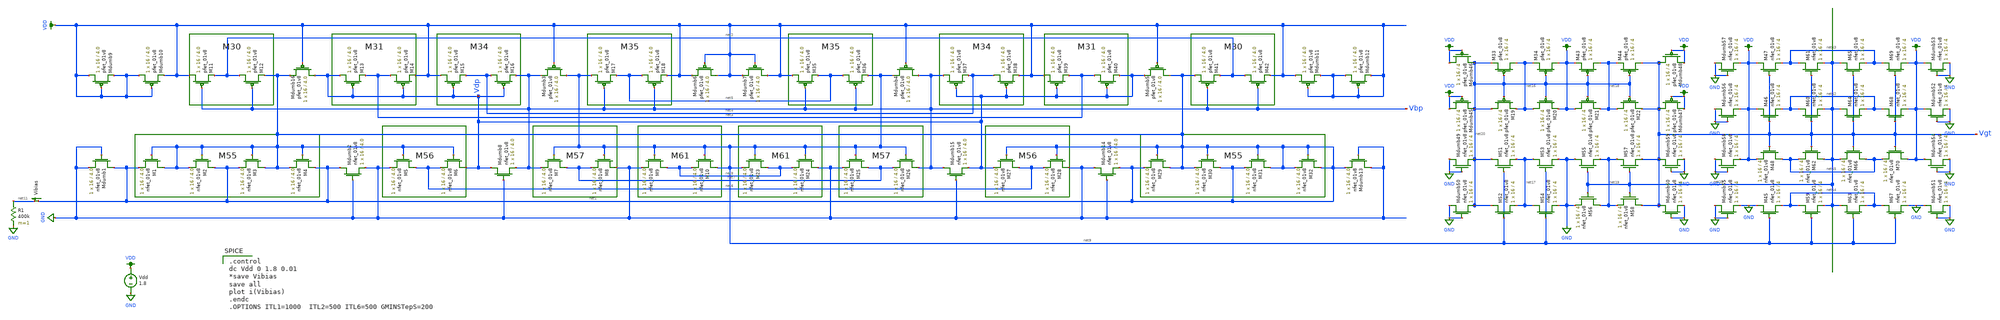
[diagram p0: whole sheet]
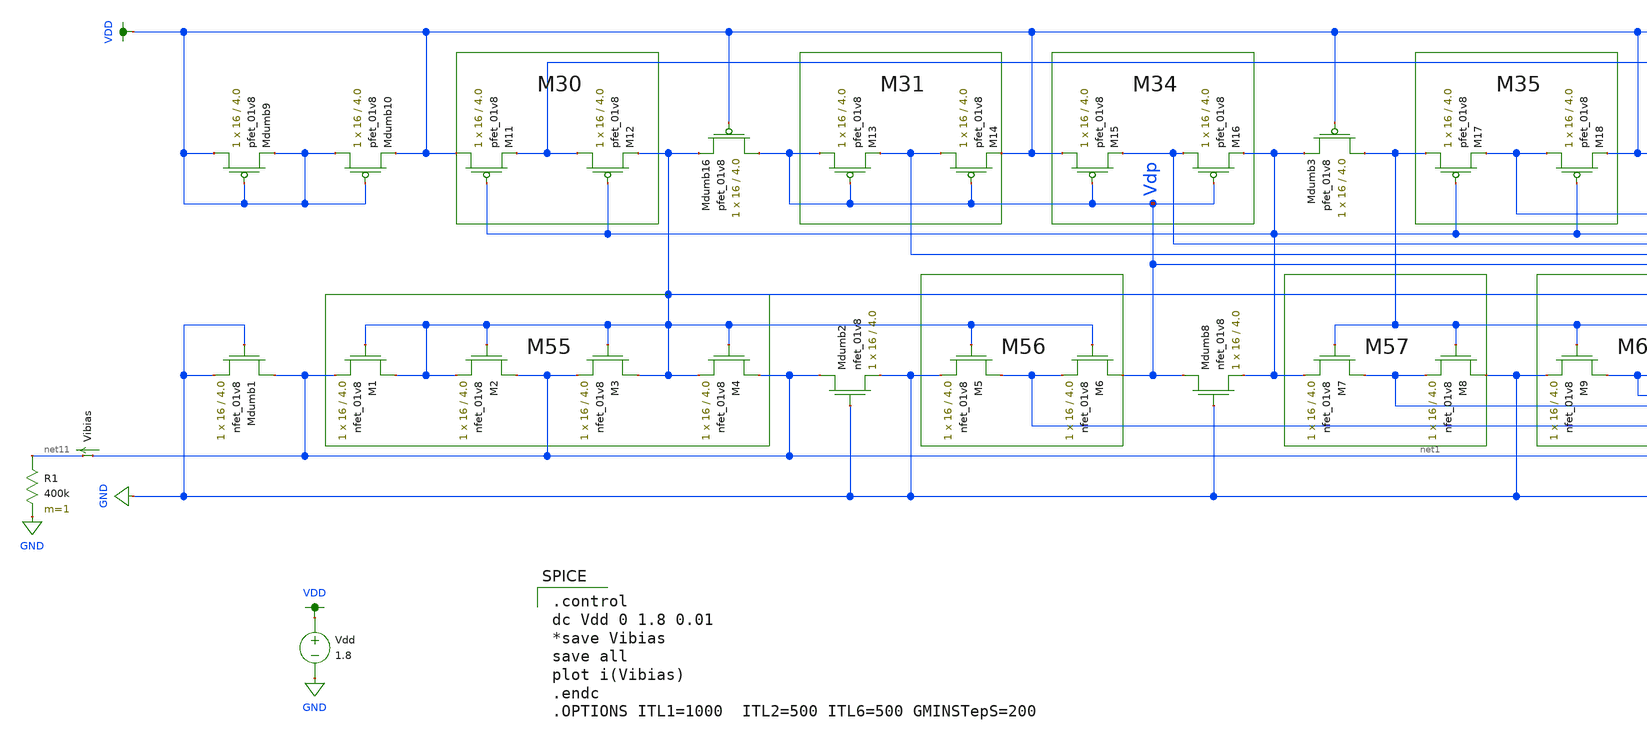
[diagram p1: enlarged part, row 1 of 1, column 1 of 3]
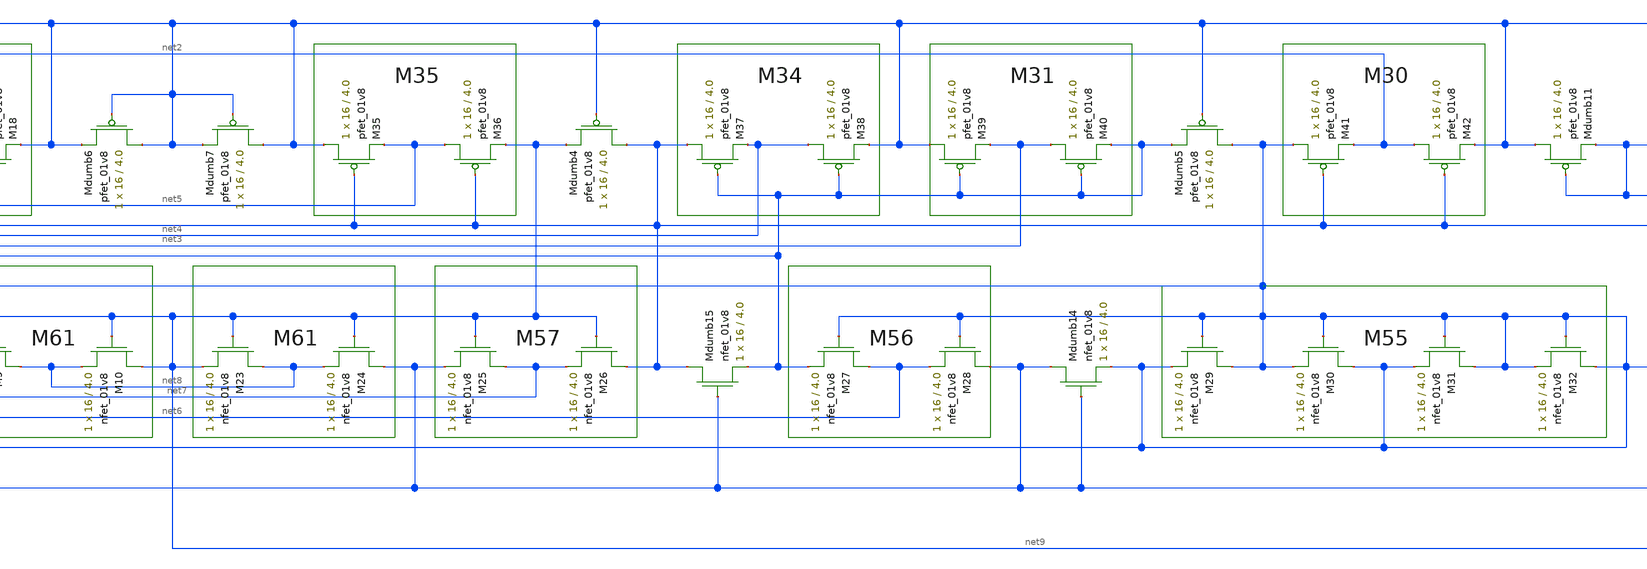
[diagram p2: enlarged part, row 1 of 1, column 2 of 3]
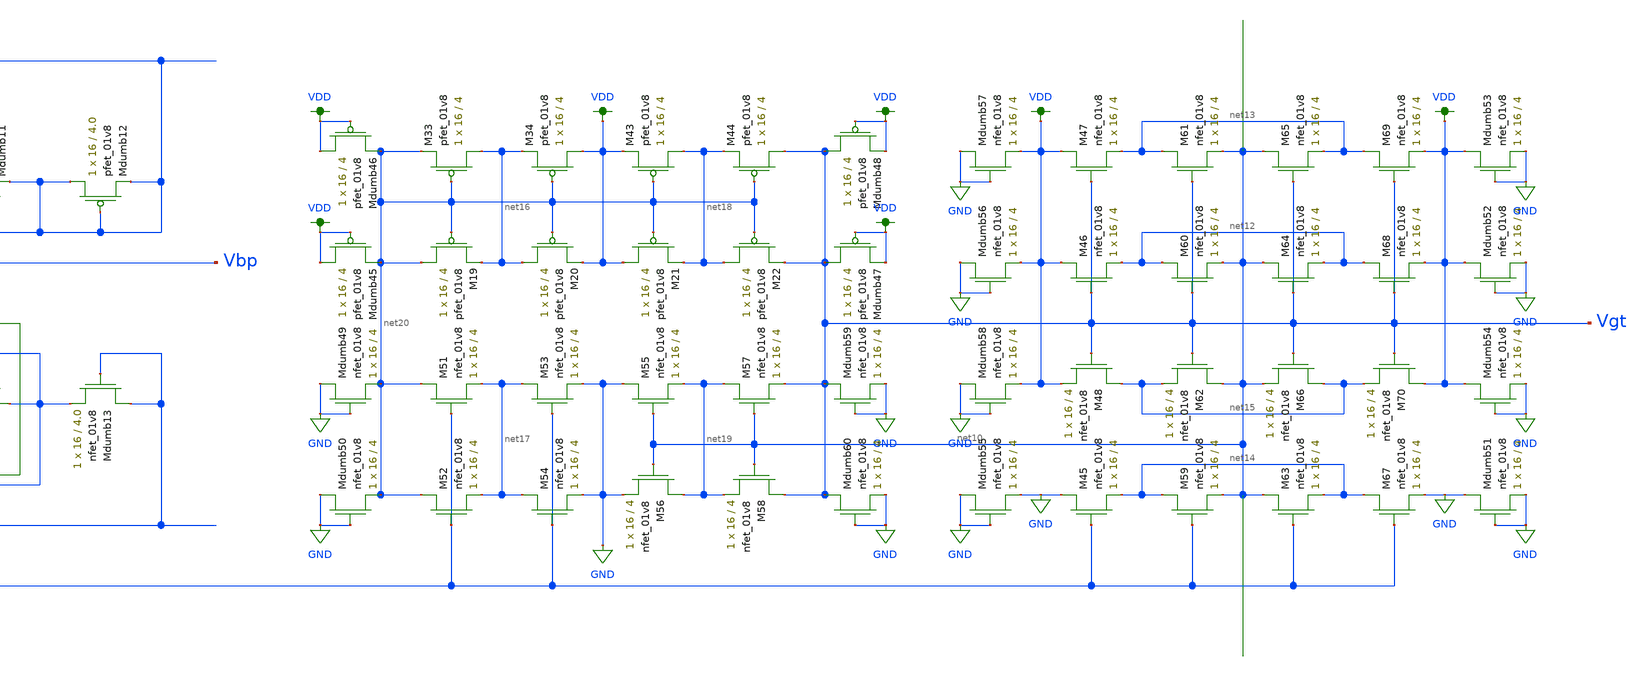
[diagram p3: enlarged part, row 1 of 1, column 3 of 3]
** sch_path: schematic/LDS/test/ibias_vgt.sch
**.subckt ibias_vgt
XM1 net1 net1 net1 GND sky130_fd_pr__nfet_01v8 L=4.0 W=16 nf=1 ad='int((nf+1)/2) * W/nf * 0.29' as='int((nf+2)/2) * W/nf * 0.29'
+ pd='2*int((nf+1)/2) * (W/nf + 0.29)' ps='2*int((nf+2)/2) * (W/nf + 0.29)' nrd='0.29 / W' nrs='0.29 / W'
+ sa=0 sb=0 sd=0 mult=1 m=1
XM2 net1 net1 net1 GND sky130_fd_pr__nfet_01v8 L=4.0 W=16 nf=1 ad='int((nf+1)/2) * W/nf * 0.29' as='int((nf+2)/2) * W/nf * 0.29'
+ pd='2*int((nf+1)/2) * (W/nf + 0.29)' ps='2*int((nf+2)/2) * (W/nf + 0.29)' nrd='0.29 / W' nrs='0.29 / W'
+ sa=0 sb=0 sd=0 mult=1 m=1
XM3 net1 net1 net1 GND sky130_fd_pr__nfet_01v8 L=4.0 W=16 nf=1 ad='int((nf+1)/2) * W/nf * 0.29' as='int((nf+2)/2) * W/nf * 0.29'
+ pd='2*int((nf+1)/2) * (W/nf + 0.29)' ps='2*int((nf+2)/2) * (W/nf + 0.29)' nrd='0.29 / W' nrs='0.29 / W'
+ sa=0 sb=0 sd=0 mult=1 m=1
XM4 net1 net1 net1 GND sky130_fd_pr__nfet_01v8 L=4.0 W=16 nf=1 ad='int((nf+1)/2) * W/nf * 0.29' as='int((nf+2)/2) * W/nf * 0.29'
+ pd='2*int((nf+1)/2) * (W/nf + 0.29)' ps='2*int((nf+2)/2) * (W/nf + 0.29)' nrd='0.29 / W' nrs='0.29 / W'
+ sa=0 sb=0 sd=0 mult=1 m=1
XM5 net6 net1 GND GND sky130_fd_pr__nfet_01v8 L=4.0 W=16 nf=1 ad='int((nf+1)/2) * W/nf * 0.29' as='int((nf+2)/2) * W/nf * 0.29'
+ pd='2*int((nf+1)/2) * (W/nf + 0.29)' ps='2*int((nf+2)/2) * (W/nf + 0.29)' nrd='0.29 / W' nrs='0.29 / W'
+ sa=0 sb=0 sd=0 mult=1 m=1
XM6 Vdp net1 net6 GND sky130_fd_pr__nfet_01v8 L=4.0 W=16 nf=1 ad='int((nf+1)/2) * W/nf * 0.29' as='int((nf+2)/2) * W/nf * 0.29'
+ pd='2*int((nf+1)/2) * (W/nf + 0.29)' ps='2*int((nf+2)/2) * (W/nf + 0.29)' nrd='0.29 / W' nrs='0.29 / W'
+ sa=0 sb=0 sd=0 mult=1 m=1
XM7 net7 net9 Vbp GND sky130_fd_pr__nfet_01v8 L=4.0 W=16 nf=1 ad='int((nf+1)/2) * W/nf * 0.29' as='int((nf+2)/2) * W/nf * 0.29'
+ pd='2*int((nf+1)/2) * (W/nf + 0.29)' ps='2*int((nf+2)/2) * (W/nf + 0.29)' nrd='0.29 / W' nrs='0.29 / W'
+ sa=0 sb=0 sd=0 mult=1 m=1
XM8 GND net9 net7 GND sky130_fd_pr__nfet_01v8 L=4.0 W=16 nf=1 ad='int((nf+1)/2) * W/nf * 0.29' as='int((nf+2)/2) * W/nf * 0.29'
+ pd='2*int((nf+1)/2) * (W/nf + 0.29)' ps='2*int((nf+2)/2) * (W/nf + 0.29)' nrd='0.29 / W' nrs='0.29 / W'
+ sa=0 sb=0 sd=0 mult=1 m=1
XM9 net8 net9 GND GND sky130_fd_pr__nfet_01v8 L=4.0 W=16 nf=1 ad='int((nf+1)/2) * W/nf * 0.29' as='int((nf+2)/2) * W/nf * 0.29'
+ pd='2*int((nf+1)/2) * (W/nf + 0.29)' ps='2*int((nf+2)/2) * (W/nf + 0.29)' nrd='0.29 / W' nrs='0.29 / W'
+ sa=0 sb=0 sd=0 mult=1 m=1
XM10 net9 net9 net8 GND sky130_fd_pr__nfet_01v8 L=4.0 W=16 nf=1 ad='int((nf+1)/2) * W/nf * 0.29' as='int((nf+2)/2) * W/nf * 0.29'
+ pd='2*int((nf+1)/2) * (W/nf + 0.29)' ps='2*int((nf+2)/2) * (W/nf + 0.29)' nrd='0.29 / W' nrs='0.29 / W'
+ sa=0 sb=0 sd=0 mult=1 m=1
XM11 VDD Vbp net2 VDD sky130_fd_pr__pfet_01v8 L=4.0 W=16 nf=1 ad='int((nf+1)/2) * W/nf * 0.29' as='int((nf+2)/2) * W/nf * 0.29'
+ pd='2*int((nf+1)/2) * (W/nf + 0.29)' ps='2*int((nf+2)/2) * (W/nf + 0.29)' nrd='0.29 / W' nrs='0.29 / W'
+ sa=0 sb=0 sd=0 mult=1 m=1
XM12 net2 Vbp net1 VDD sky130_fd_pr__pfet_01v8 L=4.0 W=16 nf=1 ad='int((nf+1)/2) * W/nf * 0.29' as='int((nf+2)/2) * W/nf * 0.29'
+ pd='2*int((nf+1)/2) * (W/nf + 0.29)' ps='2*int((nf+2)/2) * (W/nf + 0.29)' nrd='0.29 / W' nrs='0.29 / W'
+ sa=0 sb=0 sd=0 mult=1 m=1
XM13 Vdp Vdp net3 VDD sky130_fd_pr__pfet_01v8 L=4.0 W=16 nf=1 ad='int((nf+1)/2) * W/nf * 0.29' as='int((nf+2)/2) * W/nf * 0.29'
+ pd='2*int((nf+1)/2) * (W/nf + 0.29)' ps='2*int((nf+2)/2) * (W/nf + 0.29)' nrd='0.29 / W' nrs='0.29 / W'
+ sa=0 sb=0 sd=0 mult=1 m=1
XM14 net3 Vdp VDD VDD sky130_fd_pr__pfet_01v8 L=4.0 W=16 nf=1 ad='int((nf+1)/2) * W/nf * 0.29' as='int((nf+2)/2) * W/nf * 0.29'
+ pd='2*int((nf+1)/2) * (W/nf + 0.29)' ps='2*int((nf+2)/2) * (W/nf + 0.29)' nrd='0.29 / W' nrs='0.29 / W'
+ sa=0 sb=0 sd=0 mult=1 m=1
XM15 VDD Vdp net4 VDD sky130_fd_pr__pfet_01v8 L=4.0 W=16 nf=1 ad='int((nf+1)/2) * W/nf * 0.29' as='int((nf+2)/2) * W/nf * 0.29'
+ pd='2*int((nf+1)/2) * (W/nf + 0.29)' ps='2*int((nf+2)/2) * (W/nf + 0.29)' nrd='0.29 / W' nrs='0.29 / W'
+ sa=0 sb=0 sd=0 mult=1 m=1
XM16 net4 Vdp Vbp VDD sky130_fd_pr__pfet_01v8 L=4.0 W=16 nf=1 ad='int((nf+1)/2) * W/nf * 0.29' as='int((nf+2)/2) * W/nf * 0.29'
+ pd='2*int((nf+1)/2) * (W/nf + 0.29)' ps='2*int((nf+2)/2) * (W/nf + 0.29)' nrd='0.29 / W' nrs='0.29 / W'
+ sa=0 sb=0 sd=0 mult=1 m=1
XM17 net9 Vbp net5 VDD sky130_fd_pr__pfet_01v8 L=4.0 W=16 nf=1 ad='int((nf+1)/2) * W/nf * 0.29' as='int((nf+2)/2) * W/nf * 0.29'
+ pd='2*int((nf+1)/2) * (W/nf + 0.29)' ps='2*int((nf+2)/2) * (W/nf + 0.29)' nrd='0.29 / W' nrs='0.29 / W'
+ sa=0 sb=0 sd=0 mult=1 m=1
XM18 net5 Vbp VDD VDD sky130_fd_pr__pfet_01v8 L=4.0 W=16 nf=1 ad='int((nf+1)/2) * W/nf * 0.29' as='int((nf+2)/2) * W/nf * 0.29'
+ pd='2*int((nf+1)/2) * (W/nf + 0.29)' ps='2*int((nf+2)/2) * (W/nf + 0.29)' nrd='0.29 / W' nrs='0.29 / W'
+ sa=0 sb=0 sd=0 mult=1 m=1
XMdumb16 Vdp VDD net1 VDD sky130_fd_pr__pfet_01v8 L=4.0 W=16 nf=1 ad='int((nf+1)/2) * W/nf * 0.29' as='int((nf+2)/2) * W/nf * 0.29'
+ pd='2*int((nf+1)/2) * (W/nf + 0.29)' ps='2*int((nf+2)/2) * (W/nf + 0.29)' nrd='0.29 / W' nrs='0.29 / W'
+ sa=0 sb=0 sd=0 mult=1 m=1
XMdumb3 net9 VDD Vbp VDD sky130_fd_pr__pfet_01v8 L=4.0 W=16 nf=1 ad='int((nf+1)/2) * W/nf * 0.29' as='int((nf+2)/2) * W/nf * 0.29'
+ pd='2*int((nf+1)/2) * (W/nf + 0.29)' ps='2*int((nf+2)/2) * (W/nf + 0.29)' nrd='0.29 / W' nrs='0.29 / W'
+ sa=0 sb=0 sd=0 mult=1 m=1
XMdumb2 net1 GND GND GND sky130_fd_pr__nfet_01v8 L=4.0 W=16 nf=1 ad='int((nf+1)/2) * W/nf * 0.29' as='int((nf+2)/2) * W/nf * 0.29'
+ pd='2*int((nf+1)/2) * (W/nf + 0.29)' ps='2*int((nf+2)/2) * (W/nf + 0.29)' nrd='0.29 / W' nrs='0.29 / W'
+ sa=0 sb=0 sd=0 mult=1 m=1
XMdumb8 Vdp GND Vbp GND sky130_fd_pr__nfet_01v8 L=4.0 W=16 nf=1 ad='int((nf+1)/2) * W/nf * 0.29' as='int((nf+2)/2) * W/nf * 0.29'
+ pd='2*int((nf+1)/2) * (W/nf + 0.29)' ps='2*int((nf+2)/2) * (W/nf + 0.29)' nrd='0.29 / W' nrs='0.29 / W'
+ sa=0 sb=0 sd=0 mult=1 m=1
XM23 net8 net9 net9 GND sky130_fd_pr__nfet_01v8 L=4.0 W=16 nf=1 ad='int((nf+1)/2) * W/nf * 0.29' as='int((nf+2)/2) * W/nf * 0.29'
+ pd='2*int((nf+1)/2) * (W/nf + 0.29)' ps='2*int((nf+2)/2) * (W/nf + 0.29)' nrd='0.29 / W' nrs='0.29 / W'
+ sa=0 sb=0 sd=0 mult=1 m=1
XM24 GND net9 net8 GND sky130_fd_pr__nfet_01v8 L=4.0 W=16 nf=1 ad='int((nf+1)/2) * W/nf * 0.29' as='int((nf+2)/2) * W/nf * 0.29'
+ pd='2*int((nf+1)/2) * (W/nf + 0.29)' ps='2*int((nf+2)/2) * (W/nf + 0.29)' nrd='0.29 / W' nrs='0.29 / W'
+ sa=0 sb=0 sd=0 mult=1 m=1
XM25 net7 net9 GND GND sky130_fd_pr__nfet_01v8 L=4.0 W=16 nf=1 ad='int((nf+1)/2) * W/nf * 0.29' as='int((nf+2)/2) * W/nf * 0.29'
+ pd='2*int((nf+1)/2) * (W/nf + 0.29)' ps='2*int((nf+2)/2) * (W/nf + 0.29)' nrd='0.29 / W' nrs='0.29 / W'
+ sa=0 sb=0 sd=0 mult=1 m=1
XM26 Vbp net9 net7 GND sky130_fd_pr__nfet_01v8 L=4.0 W=16 nf=1 ad='int((nf+1)/2) * W/nf * 0.29' as='int((nf+2)/2) * W/nf * 0.29'
+ pd='2*int((nf+1)/2) * (W/nf + 0.29)' ps='2*int((nf+2)/2) * (W/nf + 0.29)' nrd='0.29 / W' nrs='0.29 / W'
+ sa=0 sb=0 sd=0 mult=1 m=1
XM27 net6 net1 Vdp GND sky130_fd_pr__nfet_01v8 L=4.0 W=16 nf=1 ad='int((nf+1)/2) * W/nf * 0.29' as='int((nf+2)/2) * W/nf * 0.29'
+ pd='2*int((nf+1)/2) * (W/nf + 0.29)' ps='2*int((nf+2)/2) * (W/nf + 0.29)' nrd='0.29 / W' nrs='0.29 / W'
+ sa=0 sb=0 sd=0 mult=1 m=1
XM28 GND net1 net6 GND sky130_fd_pr__nfet_01v8 L=4.0 W=16 nf=1 ad='int((nf+1)/2) * W/nf * 0.29' as='int((nf+2)/2) * W/nf * 0.29'
+ pd='2*int((nf+1)/2) * (W/nf + 0.29)' ps='2*int((nf+2)/2) * (W/nf + 0.29)' nrd='0.29 / W' nrs='0.29 / W'
+ sa=0 sb=0 sd=0 mult=1 m=1
XM29 net1 net1 net1 GND sky130_fd_pr__nfet_01v8 L=4.0 W=16 nf=1 ad='int((nf+1)/2) * W/nf * 0.29' as='int((nf+2)/2) * W/nf * 0.29'
+ pd='2*int((nf+1)/2) * (W/nf + 0.29)' ps='2*int((nf+2)/2) * (W/nf + 0.29)' nrd='0.29 / W' nrs='0.29 / W'
+ sa=0 sb=0 sd=0 mult=1 m=1
XM30 net1 net1 net1 GND sky130_fd_pr__nfet_01v8 L=4.0 W=16 nf=1 ad='int((nf+1)/2) * W/nf * 0.29' as='int((nf+2)/2) * W/nf * 0.29'
+ pd='2*int((nf+1)/2) * (W/nf + 0.29)' ps='2*int((nf+2)/2) * (W/nf + 0.29)' nrd='0.29 / W' nrs='0.29 / W'
+ sa=0 sb=0 sd=0 mult=1 m=1
XM31 net1 net1 net1 GND sky130_fd_pr__nfet_01v8 L=4.0 W=16 nf=1 ad='int((nf+1)/2) * W/nf * 0.29' as='int((nf+2)/2) * W/nf * 0.29'
+ pd='2*int((nf+1)/2) * (W/nf + 0.29)' ps='2*int((nf+2)/2) * (W/nf + 0.29)' nrd='0.29 / W' nrs='0.29 / W'
+ sa=0 sb=0 sd=0 mult=1 m=1
XM32 net1 net1 net1 GND sky130_fd_pr__nfet_01v8 L=4.0 W=16 nf=1 ad='int((nf+1)/2) * W/nf * 0.29' as='int((nf+2)/2) * W/nf * 0.29'
+ pd='2*int((nf+1)/2) * (W/nf + 0.29)' ps='2*int((nf+2)/2) * (W/nf + 0.29)' nrd='0.29 / W' nrs='0.29 / W'
+ sa=0 sb=0 sd=0 mult=1 m=1
XMdumb15 Vbp GND Vdp GND sky130_fd_pr__nfet_01v8 L=4.0 W=16 nf=1 ad='int((nf+1)/2) * W/nf * 0.29' as='int((nf+2)/2) * W/nf * 0.29'
+ pd='2*int((nf+1)/2) * (W/nf + 0.29)' ps='2*int((nf+2)/2) * (W/nf + 0.29)' nrd='0.29 / W' nrs='0.29 / W'
+ sa=0 sb=0 sd=0 mult=1 m=1
XMdumb14 GND GND net1 GND sky130_fd_pr__nfet_01v8 L=4.0 W=16 nf=1 ad='int((nf+1)/2) * W/nf * 0.29' as='int((nf+2)/2) * W/nf * 0.29'
+ pd='2*int((nf+1)/2) * (W/nf + 0.29)' ps='2*int((nf+2)/2) * (W/nf + 0.29)' nrd='0.29 / W' nrs='0.29 / W'
+ sa=0 sb=0 sd=0 mult=1 m=1
XM35 VDD Vbp net5 VDD sky130_fd_pr__pfet_01v8 L=4.0 W=16 nf=1 ad='int((nf+1)/2) * W/nf * 0.29' as='int((nf+2)/2) * W/nf * 0.29'
+ pd='2*int((nf+1)/2) * (W/nf + 0.29)' ps='2*int((nf+2)/2) * (W/nf + 0.29)' nrd='0.29 / W' nrs='0.29 / W'
+ sa=0 sb=0 sd=0 mult=1 m=1
XM36 net5 Vbp net9 VDD sky130_fd_pr__pfet_01v8 L=4.0 W=16 nf=1 ad='int((nf+1)/2) * W/nf * 0.29' as='int((nf+2)/2) * W/nf * 0.29'
+ pd='2*int((nf+1)/2) * (W/nf + 0.29)' ps='2*int((nf+2)/2) * (W/nf + 0.29)' nrd='0.29 / W' nrs='0.29 / W'
+ sa=0 sb=0 sd=0 mult=1 m=1
XM37 Vbp Vdp net4 VDD sky130_fd_pr__pfet_01v8 L=4.0 W=16 nf=1 ad='int((nf+1)/2) * W/nf * 0.29' as='int((nf+2)/2) * W/nf * 0.29'
+ pd='2*int((nf+1)/2) * (W/nf + 0.29)' ps='2*int((nf+2)/2) * (W/nf + 0.29)' nrd='0.29 / W' nrs='0.29 / W'
+ sa=0 sb=0 sd=0 mult=1 m=1
XM38 net4 Vdp VDD VDD sky130_fd_pr__pfet_01v8 L=4.0 W=16 nf=1 ad='int((nf+1)/2) * W/nf * 0.29' as='int((nf+2)/2) * W/nf * 0.29'
+ pd='2*int((nf+1)/2) * (W/nf + 0.29)' ps='2*int((nf+2)/2) * (W/nf + 0.29)' nrd='0.29 / W' nrs='0.29 / W'
+ sa=0 sb=0 sd=0 mult=1 m=1
XM39 VDD Vdp net3 VDD sky130_fd_pr__pfet_01v8 L=4.0 W=16 nf=1 ad='int((nf+1)/2) * W/nf * 0.29' as='int((nf+2)/2) * W/nf * 0.29'
+ pd='2*int((nf+1)/2) * (W/nf + 0.29)' ps='2*int((nf+2)/2) * (W/nf + 0.29)' nrd='0.29 / W' nrs='0.29 / W'
+ sa=0 sb=0 sd=0 mult=1 m=1
XM40 net3 Vdp Vdp VDD sky130_fd_pr__pfet_01v8 L=4.0 W=16 nf=1 ad='int((nf+1)/2) * W/nf * 0.29' as='int((nf+2)/2) * W/nf * 0.29'
+ pd='2*int((nf+1)/2) * (W/nf + 0.29)' ps='2*int((nf+2)/2) * (W/nf + 0.29)' nrd='0.29 / W' nrs='0.29 / W'
+ sa=0 sb=0 sd=0 mult=1 m=1
XM41 net1 Vbp net2 VDD sky130_fd_pr__pfet_01v8 L=4.0 W=16 nf=1 ad='int((nf+1)/2) * W/nf * 0.29' as='int((nf+2)/2) * W/nf * 0.29'
+ pd='2*int((nf+1)/2) * (W/nf + 0.29)' ps='2*int((nf+2)/2) * (W/nf + 0.29)' nrd='0.29 / W' nrs='0.29 / W'
+ sa=0 sb=0 sd=0 mult=1 m=1
XM42 net2 Vbp VDD VDD sky130_fd_pr__pfet_01v8 L=4.0 W=16 nf=1 ad='int((nf+1)/2) * W/nf * 0.29' as='int((nf+2)/2) * W/nf * 0.29'
+ pd='2*int((nf+1)/2) * (W/nf + 0.29)' ps='2*int((nf+2)/2) * (W/nf + 0.29)' nrd='0.29 / W' nrs='0.29 / W'
+ sa=0 sb=0 sd=0 mult=1 m=1
XMdumb4 Vbp VDD net9 VDD sky130_fd_pr__pfet_01v8 L=4.0 W=16 nf=1 ad='int((nf+1)/2) * W/nf * 0.29' as='int((nf+2)/2) * W/nf * 0.29'
+ pd='2*int((nf+1)/2) * (W/nf + 0.29)' ps='2*int((nf+2)/2) * (W/nf + 0.29)' nrd='0.29 / W' nrs='0.29 / W'
+ sa=0 sb=0 sd=0 mult=1 m=1
XMdumb5 net1 VDD Vdp VDD sky130_fd_pr__pfet_01v8 L=4.0 W=16 nf=1 ad='int((nf+1)/2) * W/nf * 0.29' as='int((nf+2)/2) * W/nf * 0.29'
+ pd='2*int((nf+1)/2) * (W/nf + 0.29)' ps='2*int((nf+2)/2) * (W/nf + 0.29)' nrd='0.29 / W' nrs='0.29 / W'
+ sa=0 sb=0 sd=0 mult=1 m=1
XMdumb6 VDD VDD VDD VDD sky130_fd_pr__pfet_01v8 L=4.0 W=16 nf=1 ad='int((nf+1)/2) * W/nf * 0.29' as='int((nf+2)/2) * W/nf * 0.29'
+ pd='2*int((nf+1)/2) * (W/nf + 0.29)' ps='2*int((nf+2)/2) * (W/nf + 0.29)' nrd='0.29 / W' nrs='0.29 / W'
+ sa=0 sb=0 sd=0 mult=1 m=1
XMdumb7 VDD VDD VDD VDD sky130_fd_pr__pfet_01v8 L=4.0 W=16 nf=1 ad='int((nf+1)/2) * W/nf * 0.29' as='int((nf+2)/2) * W/nf * 0.29'
+ pd='2*int((nf+1)/2) * (W/nf + 0.29)' ps='2*int((nf+2)/2) * (W/nf + 0.29)' nrd='0.29 / W' nrs='0.29 / W'
+ sa=0 sb=0 sd=0 mult=1 m=1
XMdumb11 VDD VDD VDD VDD sky130_fd_pr__pfet_01v8 L=4.0 W=16 nf=1 ad='int((nf+1)/2) * W/nf * 0.29' as='int((nf+2)/2) * W/nf * 0.29'
+ pd='2*int((nf+1)/2) * (W/nf + 0.29)' ps='2*int((nf+2)/2) * (W/nf + 0.29)' nrd='0.29 / W' nrs='0.29 / W'
+ sa=0 sb=0 sd=0 mult=1 m=1
XMdumb12 VDD VDD VDD VDD sky130_fd_pr__pfet_01v8 L=4.0 W=16 nf=1 ad='int((nf+1)/2) * W/nf * 0.29' as='int((nf+2)/2) * W/nf * 0.29'
+ pd='2*int((nf+1)/2) * (W/nf + 0.29)' ps='2*int((nf+2)/2) * (W/nf + 0.29)' nrd='0.29 / W' nrs='0.29 / W'
+ sa=0 sb=0 sd=0 mult=1 m=1
XMdumb13 GND GND net1 GND sky130_fd_pr__nfet_01v8 L=4.0 W=16 nf=1 ad='int((nf+1)/2) * W/nf * 0.29' as='int((nf+2)/2) * W/nf * 0.29'
+ pd='2*int((nf+1)/2) * (W/nf + 0.29)' ps='2*int((nf+2)/2) * (W/nf + 0.29)' nrd='0.29 / W' nrs='0.29 / W'
+ sa=0 sb=0 sd=0 mult=1 m=1
XMdumb1 net1 GND GND GND sky130_fd_pr__nfet_01v8 L=4.0 W=16 nf=1 ad='int((nf+1)/2) * W/nf * 0.29' as='int((nf+2)/2) * W/nf * 0.29'
+ pd='2*int((nf+1)/2) * (W/nf + 0.29)' ps='2*int((nf+2)/2) * (W/nf + 0.29)' nrd='0.29 / W' nrs='0.29 / W'
+ sa=0 sb=0 sd=0 mult=1 m=1
XMdumb10 VDD VDD VDD VDD sky130_fd_pr__pfet_01v8 L=4.0 W=16 nf=1 ad='int((nf+1)/2) * W/nf * 0.29' as='int((nf+2)/2) * W/nf * 0.29'
+ pd='2*int((nf+1)/2) * (W/nf + 0.29)' ps='2*int((nf+2)/2) * (W/nf + 0.29)' nrd='0.29 / W' nrs='0.29 / W'
+ sa=0 sb=0 sd=0 mult=1 m=1
XMdumb9 VDD VDD VDD VDD sky130_fd_pr__pfet_01v8 L=4.0 W=16 nf=1 ad='int((nf+1)/2) * W/nf * 0.29' as='int((nf+2)/2) * W/nf * 0.29'
+ pd='2*int((nf+1)/2) * (W/nf + 0.29)' ps='2*int((nf+2)/2) * (W/nf + 0.29)' nrd='0.29 / W' nrs='0.29 / W'
+ sa=0 sb=0 sd=0 mult=1 m=1
Vdd VDD GND 1.8
R1 net11 GND 400k m=1
Vibias net1 net11 0
.save i(vibias)
XM45 GND net9 net14 GND sky130_fd_pr__nfet_01v8 L=4 W=16 nf=1 ad='int((nf+1)/2) * W/nf * 0.29' as='int((nf+2)/2) * W/nf * 0.29'
+ pd='2*int((nf+1)/2) * (W/nf + 0.29)' ps='2*int((nf+2)/2) * (W/nf + 0.29)' nrd='0.29 / W' nrs='0.29 / W'
+ sa=0 sb=0 sd=0 mult=1 m=1
XM46 VDD Vgt net12 GND sky130_fd_pr__nfet_01v8 L=4 W=16 nf=1 ad='int((nf+1)/2) * W/nf * 0.29' as='int((nf+2)/2) * W/nf * 0.29'
+ pd='2*int((nf+1)/2) * (W/nf + 0.29)' ps='2*int((nf+2)/2) * (W/nf + 0.29)' nrd='0.29 / W' nrs='0.29 / W'
+ sa=0 sb=0 sd=0 mult=1 m=1
XM47 VDD Vgt net13 GND sky130_fd_pr__nfet_01v8 L=4 W=16 nf=1 ad='int((nf+1)/2) * W/nf * 0.29' as='int((nf+2)/2) * W/nf * 0.29'
+ pd='2*int((nf+1)/2) * (W/nf + 0.29)' ps='2*int((nf+2)/2) * (W/nf + 0.29)' nrd='0.29 / W' nrs='0.29 / W'
+ sa=0 sb=0 sd=0 mult=1 m=1
XM48 net15 Vgt VDD GND sky130_fd_pr__nfet_01v8 L=4 W=16 nf=1 ad='int((nf+1)/2) * W/nf * 0.29' as='int((nf+2)/2) * W/nf * 0.29'
+ pd='2*int((nf+1)/2) * (W/nf + 0.29)' ps='2*int((nf+2)/2) * (W/nf + 0.29)' nrd='0.29 / W' nrs='0.29 / W'
+ sa=0 sb=0 sd=0 mult=1 m=1
XMdumb51 GND GND GND GND sky130_fd_pr__nfet_01v8 L=4 W=16 nf=1 ad='int((nf+1)/2) * W/nf * 0.29' as='int((nf+2)/2) * W/nf * 0.29'
+ pd='2*int((nf+1)/2) * (W/nf + 0.29)' ps='2*int((nf+2)/2) * (W/nf + 0.29)' nrd='0.29 / W' nrs='0.29 / W'
+ sa=0 sb=0 sd=0 mult=1 m=1
XMdumb52 VDD GND GND GND sky130_fd_pr__nfet_01v8 L=4 W=16 nf=1 ad='int((nf+1)/2) * W/nf * 0.29' as='int((nf+2)/2) * W/nf * 0.29'
+ pd='2*int((nf+1)/2) * (W/nf + 0.29)' ps='2*int((nf+2)/2) * (W/nf + 0.29)' nrd='0.29 / W' nrs='0.29 / W'
+ sa=0 sb=0 sd=0 mult=1 m=1
XMdumb53 VDD GND GND GND sky130_fd_pr__nfet_01v8 L=4 W=16 nf=1 ad='int((nf+1)/2) * W/nf * 0.29' as='int((nf+2)/2) * W/nf * 0.29'
+ pd='2*int((nf+1)/2) * (W/nf + 0.29)' ps='2*int((nf+2)/2) * (W/nf + 0.29)' nrd='0.29 / W' nrs='0.29 / W'
+ sa=0 sb=0 sd=0 mult=1 m=1
XMdumb54 VDD GND GND GND sky130_fd_pr__nfet_01v8 L=4 W=16 nf=1 ad='int((nf+1)/2) * W/nf * 0.29' as='int((nf+2)/2) * W/nf * 0.29'
+ pd='2*int((nf+1)/2) * (W/nf + 0.29)' ps='2*int((nf+2)/2) * (W/nf + 0.29)' nrd='0.29 / W' nrs='0.29 / W'
+ sa=0 sb=0 sd=0 mult=1 m=1
XMdumb55 GND GND GND GND sky130_fd_pr__nfet_01v8 L=4 W=16 nf=1 ad='int((nf+1)/2) * W/nf * 0.29' as='int((nf+2)/2) * W/nf * 0.29'
+ pd='2*int((nf+1)/2) * (W/nf + 0.29)' ps='2*int((nf+2)/2) * (W/nf + 0.29)' nrd='0.29 / W' nrs='0.29 / W'
+ sa=0 sb=0 sd=0 mult=1 m=1
XMdumb56 GND GND VDD GND sky130_fd_pr__nfet_01v8 L=4 W=16 nf=1 ad='int((nf+1)/2) * W/nf * 0.29' as='int((nf+2)/2) * W/nf * 0.29'
+ pd='2*int((nf+1)/2) * (W/nf + 0.29)' ps='2*int((nf+2)/2) * (W/nf + 0.29)' nrd='0.29 / W' nrs='0.29 / W'
+ sa=0 sb=0 sd=0 mult=1 m=1
XMdumb57 GND GND VDD GND sky130_fd_pr__nfet_01v8 L=4 W=16 nf=1 ad='int((nf+1)/2) * W/nf * 0.29' as='int((nf+2)/2) * W/nf * 0.29'
+ pd='2*int((nf+1)/2) * (W/nf + 0.29)' ps='2*int((nf+2)/2) * (W/nf + 0.29)' nrd='0.29 / W' nrs='0.29 / W'
+ sa=0 sb=0 sd=0 mult=1 m=1
XMdumb58 GND GND VDD GND sky130_fd_pr__nfet_01v8 L=4 W=16 nf=1 ad='int((nf+1)/2) * W/nf * 0.29' as='int((nf+2)/2) * W/nf * 0.29'
+ pd='2*int((nf+1)/2) * (W/nf + 0.29)' ps='2*int((nf+2)/2) * (W/nf + 0.29)' nrd='0.29 / W' nrs='0.29 / W'
+ sa=0 sb=0 sd=0 mult=1 m=1
XM59 net14 net9 net10 GND sky130_fd_pr__nfet_01v8 L=4 W=16 nf=1 ad='int((nf+1)/2) * W/nf * 0.29' as='int((nf+2)/2) * W/nf * 0.29'
+ pd='2*int((nf+1)/2) * (W/nf + 0.29)' ps='2*int((nf+2)/2) * (W/nf + 0.29)' nrd='0.29 / W' nrs='0.29 / W'
+ sa=0 sb=0 sd=0 mult=1 m=1
XM60 net12 Vgt net10 GND sky130_fd_pr__nfet_01v8 L=4 W=16 nf=1 ad='int((nf+1)/2) * W/nf * 0.29' as='int((nf+2)/2) * W/nf * 0.29'
+ pd='2*int((nf+1)/2) * (W/nf + 0.29)' ps='2*int((nf+2)/2) * (W/nf + 0.29)' nrd='0.29 / W' nrs='0.29 / W'
+ sa=0 sb=0 sd=0 mult=1 m=1
XM61 net13 Vgt net10 GND sky130_fd_pr__nfet_01v8 L=4 W=16 nf=1 ad='int((nf+1)/2) * W/nf * 0.29' as='int((nf+2)/2) * W/nf * 0.29'
+ pd='2*int((nf+1)/2) * (W/nf + 0.29)' ps='2*int((nf+2)/2) * (W/nf + 0.29)' nrd='0.29 / W' nrs='0.29 / W'
+ sa=0 sb=0 sd=0 mult=1 m=1
XM62 net10 Vgt net15 GND sky130_fd_pr__nfet_01v8 L=4 W=16 nf=1 ad='int((nf+1)/2) * W/nf * 0.29' as='int((nf+2)/2) * W/nf * 0.29'
+ pd='2*int((nf+1)/2) * (W/nf + 0.29)' ps='2*int((nf+2)/2) * (W/nf + 0.29)' nrd='0.29 / W' nrs='0.29 / W'
+ sa=0 sb=0 sd=0 mult=1 m=1
XM63 net10 net9 net14 GND sky130_fd_pr__nfet_01v8 L=4 W=16 nf=1 ad='int((nf+1)/2) * W/nf * 0.29' as='int((nf+2)/2) * W/nf * 0.29'
+ pd='2*int((nf+1)/2) * (W/nf + 0.29)' ps='2*int((nf+2)/2) * (W/nf + 0.29)' nrd='0.29 / W' nrs='0.29 / W'
+ sa=0 sb=0 sd=0 mult=1 m=1
XM64 net10 Vgt net12 GND sky130_fd_pr__nfet_01v8 L=4 W=16 nf=1 ad='int((nf+1)/2) * W/nf * 0.29' as='int((nf+2)/2) * W/nf * 0.29'
+ pd='2*int((nf+1)/2) * (W/nf + 0.29)' ps='2*int((nf+2)/2) * (W/nf + 0.29)' nrd='0.29 / W' nrs='0.29 / W'
+ sa=0 sb=0 sd=0 mult=1 m=1
XM65 net10 Vgt net13 GND sky130_fd_pr__nfet_01v8 L=4 W=16 nf=1 ad='int((nf+1)/2) * W/nf * 0.29' as='int((nf+2)/2) * W/nf * 0.29'
+ pd='2*int((nf+1)/2) * (W/nf + 0.29)' ps='2*int((nf+2)/2) * (W/nf + 0.29)' nrd='0.29 / W' nrs='0.29 / W'
+ sa=0 sb=0 sd=0 mult=1 m=1
XM66 net15 Vgt net10 GND sky130_fd_pr__nfet_01v8 L=4 W=16 nf=1 ad='int((nf+1)/2) * W/nf * 0.29' as='int((nf+2)/2) * W/nf * 0.29'
+ pd='2*int((nf+1)/2) * (W/nf + 0.29)' ps='2*int((nf+2)/2) * (W/nf + 0.29)' nrd='0.29 / W' nrs='0.29 / W'
+ sa=0 sb=0 sd=0 mult=1 m=1
XM67 net14 net9 GND GND sky130_fd_pr__nfet_01v8 L=4 W=16 nf=1 ad='int((nf+1)/2) * W/nf * 0.29' as='int((nf+2)/2) * W/nf * 0.29'
+ pd='2*int((nf+1)/2) * (W/nf + 0.29)' ps='2*int((nf+2)/2) * (W/nf + 0.29)' nrd='0.29 / W' nrs='0.29 / W'
+ sa=0 sb=0 sd=0 mult=1 m=1
XM68 net12 Vgt VDD GND sky130_fd_pr__nfet_01v8 L=4 W=16 nf=1 ad='int((nf+1)/2) * W/nf * 0.29' as='int((nf+2)/2) * W/nf * 0.29'
+ pd='2*int((nf+1)/2) * (W/nf + 0.29)' ps='2*int((nf+2)/2) * (W/nf + 0.29)' nrd='0.29 / W' nrs='0.29 / W'
+ sa=0 sb=0 sd=0 mult=1 m=1
XM69 net13 Vgt VDD GND sky130_fd_pr__nfet_01v8 L=4 W=16 nf=1 ad='int((nf+1)/2) * W/nf * 0.29' as='int((nf+2)/2) * W/nf * 0.29'
+ pd='2*int((nf+1)/2) * (W/nf + 0.29)' ps='2*int((nf+2)/2) * (W/nf + 0.29)' nrd='0.29 / W' nrs='0.29 / W'
+ sa=0 sb=0 sd=0 mult=1 m=1
XM70 VDD Vgt net15 GND sky130_fd_pr__nfet_01v8 L=4 W=16 nf=1 ad='int((nf+1)/2) * W/nf * 0.29' as='int((nf+2)/2) * W/nf * 0.29'
+ pd='2*int((nf+1)/2) * (W/nf + 0.29)' ps='2*int((nf+2)/2) * (W/nf + 0.29)' nrd='0.29 / W' nrs='0.29 / W'
+ sa=0 sb=0 sd=0 mult=1 m=1
XM19 net20 net20 net16 VDD sky130_fd_pr__pfet_01v8 L=4 W=16 nf=1 ad='int((nf+1)/2) * W/nf * 0.29' as='int((nf+2)/2) * W/nf * 0.29'
+ pd='2*int((nf+1)/2) * (W/nf + 0.29)' ps='2*int((nf+2)/2) * (W/nf + 0.29)' nrd='0.29 / W' nrs='0.29 / W'
+ sa=0 sb=0 sd=0 mult=1 m=1
XM20 net16 net20 VDD VDD sky130_fd_pr__pfet_01v8 L=4 W=16 nf=1 ad='int((nf+1)/2) * W/nf * 0.29' as='int((nf+2)/2) * W/nf * 0.29'
+ pd='2*int((nf+1)/2) * (W/nf + 0.29)' ps='2*int((nf+2)/2) * (W/nf + 0.29)' nrd='0.29 / W' nrs='0.29 / W'
+ sa=0 sb=0 sd=0 mult=1 m=1
XM21 VDD net20 net18 VDD sky130_fd_pr__pfet_01v8 L=4 W=16 nf=1 ad='int((nf+1)/2) * W/nf * 0.29' as='int((nf+2)/2) * W/nf * 0.29'
+ pd='2*int((nf+1)/2) * (W/nf + 0.29)' ps='2*int((nf+2)/2) * (W/nf + 0.29)' nrd='0.29 / W' nrs='0.29 / W'
+ sa=0 sb=0 sd=0 mult=1 m=1
XM22 net18 net20 Vgt VDD sky130_fd_pr__pfet_01v8 L=4 W=16 nf=1 ad='int((nf+1)/2) * W/nf * 0.29' as='int((nf+2)/2) * W/nf * 0.29'
+ pd='2*int((nf+1)/2) * (W/nf + 0.29)' ps='2*int((nf+2)/2) * (W/nf + 0.29)' nrd='0.29 / W' nrs='0.29 / W'
+ sa=0 sb=0 sd=0 mult=1 m=1
XM33 net16 net20 net20 VDD sky130_fd_pr__pfet_01v8 L=4 W=16 nf=1 ad='int((nf+1)/2) * W/nf * 0.29' as='int((nf+2)/2) * W/nf * 0.29'
+ pd='2*int((nf+1)/2) * (W/nf + 0.29)' ps='2*int((nf+2)/2) * (W/nf + 0.29)' nrd='0.29 / W' nrs='0.29 / W'
+ sa=0 sb=0 sd=0 mult=1 m=1
XM34 VDD net20 net16 VDD sky130_fd_pr__pfet_01v8 L=4 W=16 nf=1 ad='int((nf+1)/2) * W/nf * 0.29' as='int((nf+2)/2) * W/nf * 0.29'
+ pd='2*int((nf+1)/2) * (W/nf + 0.29)' ps='2*int((nf+2)/2) * (W/nf + 0.29)' nrd='0.29 / W' nrs='0.29 / W'
+ sa=0 sb=0 sd=0 mult=1 m=1
XM43 net18 net20 VDD VDD sky130_fd_pr__pfet_01v8 L=4 W=16 nf=1 ad='int((nf+1)/2) * W/nf * 0.29' as='int((nf+2)/2) * W/nf * 0.29'
+ pd='2*int((nf+1)/2) * (W/nf + 0.29)' ps='2*int((nf+2)/2) * (W/nf + 0.29)' nrd='0.29 / W' nrs='0.29 / W'
+ sa=0 sb=0 sd=0 mult=1 m=1
XM44 Vgt net20 net18 VDD sky130_fd_pr__pfet_01v8 L=4 W=16 nf=1 ad='int((nf+1)/2) * W/nf * 0.29' as='int((nf+2)/2) * W/nf * 0.29'
+ pd='2*int((nf+1)/2) * (W/nf + 0.29)' ps='2*int((nf+2)/2) * (W/nf + 0.29)' nrd='0.29 / W' nrs='0.29 / W'
+ sa=0 sb=0 sd=0 mult=1 m=1
XMdumb45 VDD VDD net20 VDD sky130_fd_pr__pfet_01v8 L=4 W=16 nf=1 ad='int((nf+1)/2) * W/nf * 0.29' as='int((nf+2)/2) * W/nf * 0.29'
+ pd='2*int((nf+1)/2) * (W/nf + 0.29)' ps='2*int((nf+2)/2) * (W/nf + 0.29)' nrd='0.29 / W' nrs='0.29 / W'
+ sa=0 sb=0 sd=0 mult=1 m=1
XMdumb46 VDD VDD net20 VDD sky130_fd_pr__pfet_01v8 L=4 W=16 nf=1 ad='int((nf+1)/2) * W/nf * 0.29' as='int((nf+2)/2) * W/nf * 0.29'
+ pd='2*int((nf+1)/2) * (W/nf + 0.29)' ps='2*int((nf+2)/2) * (W/nf + 0.29)' nrd='0.29 / W' nrs='0.29 / W'
+ sa=0 sb=0 sd=0 mult=1 m=1
XMdumb47 Vgt VDD VDD VDD sky130_fd_pr__pfet_01v8 L=4 W=16 nf=1 ad='int((nf+1)/2) * W/nf * 0.29' as='int((nf+2)/2) * W/nf * 0.29'
+ pd='2*int((nf+1)/2) * (W/nf + 0.29)' ps='2*int((nf+2)/2) * (W/nf + 0.29)' nrd='0.29 / W' nrs='0.29 / W'
+ sa=0 sb=0 sd=0 mult=1 m=1
XMdumb48 Vgt VDD VDD VDD sky130_fd_pr__pfet_01v8 L=4 W=16 nf=1 ad='int((nf+1)/2) * W/nf * 0.29' as='int((nf+2)/2) * W/nf * 0.29'
+ pd='2*int((nf+1)/2) * (W/nf + 0.29)' ps='2*int((nf+2)/2) * (W/nf + 0.29)' nrd='0.29 / W' nrs='0.29 / W'
+ sa=0 sb=0 sd=0 mult=1 m=1
XMdumb49 GND GND net20 GND sky130_fd_pr__nfet_01v8 L=4 W=16 nf=1 ad='int((nf+1)/2) * W/nf * 0.29' as='int((nf+2)/2) * W/nf * 0.29'
+ pd='2*int((nf+1)/2) * (W/nf + 0.29)' ps='2*int((nf+2)/2) * (W/nf + 0.29)' nrd='0.29 / W' nrs='0.29 / W'
+ sa=0 sb=0 sd=0 mult=1 m=1
XMdumb50 GND GND net20 GND sky130_fd_pr__nfet_01v8 L=4 W=16 nf=1 ad='int((nf+1)/2) * W/nf * 0.29' as='int((nf+2)/2) * W/nf * 0.29'
+ pd='2*int((nf+1)/2) * (W/nf + 0.29)' ps='2*int((nf+2)/2) * (W/nf + 0.29)' nrd='0.29 / W' nrs='0.29 / W'
+ sa=0 sb=0 sd=0 mult=1 m=1
XM51 net20 net9 net17 GND sky130_fd_pr__nfet_01v8 L=4 W=16 nf=1 ad='int((nf+1)/2) * W/nf * 0.29' as='int((nf+2)/2) * W/nf * 0.29'
+ pd='2*int((nf+1)/2) * (W/nf + 0.29)' ps='2*int((nf+2)/2) * (W/nf + 0.29)' nrd='0.29 / W' nrs='0.29 / W'
+ sa=0 sb=0 sd=0 mult=1 m=1
XM52 net20 net9 net17 GND sky130_fd_pr__nfet_01v8 L=4 W=16 nf=1 ad='int((nf+1)/2) * W/nf * 0.29' as='int((nf+2)/2) * W/nf * 0.29'
+ pd='2*int((nf+1)/2) * (W/nf + 0.29)' ps='2*int((nf+2)/2) * (W/nf + 0.29)' nrd='0.29 / W' nrs='0.29 / W'
+ sa=0 sb=0 sd=0 mult=1 m=1
XM53 net17 net9 GND GND sky130_fd_pr__nfet_01v8 L=4 W=16 nf=1 ad='int((nf+1)/2) * W/nf * 0.29' as='int((nf+2)/2) * W/nf * 0.29'
+ pd='2*int((nf+1)/2) * (W/nf + 0.29)' ps='2*int((nf+2)/2) * (W/nf + 0.29)' nrd='0.29 / W' nrs='0.29 / W'
+ sa=0 sb=0 sd=0 mult=1 m=1
XM54 net17 net9 GND GND sky130_fd_pr__nfet_01v8 L=4 W=16 nf=1 ad='int((nf+1)/2) * W/nf * 0.29' as='int((nf+2)/2) * W/nf * 0.29'
+ pd='2*int((nf+1)/2) * (W/nf + 0.29)' ps='2*int((nf+2)/2) * (W/nf + 0.29)' nrd='0.29 / W' nrs='0.29 / W'
+ sa=0 sb=0 sd=0 mult=1 m=1
XM55 GND net10 net19 GND sky130_fd_pr__nfet_01v8 L=4 W=16 nf=1 ad='int((nf+1)/2) * W/nf * 0.29' as='int((nf+2)/2) * W/nf * 0.29'
+ pd='2*int((nf+1)/2) * (W/nf + 0.29)' ps='2*int((nf+2)/2) * (W/nf + 0.29)' nrd='0.29 / W' nrs='0.29 / W'
+ sa=0 sb=0 sd=0 mult=1 m=1
XM56 net19 net10 GND GND sky130_fd_pr__nfet_01v8 L=4 W=16 nf=1 ad='int((nf+1)/2) * W/nf * 0.29' as='int((nf+2)/2) * W/nf * 0.29'
+ pd='2*int((nf+1)/2) * (W/nf + 0.29)' ps='2*int((nf+2)/2) * (W/nf + 0.29)' nrd='0.29 / W' nrs='0.29 / W'
+ sa=0 sb=0 sd=0 mult=1 m=1
XM57 net19 net10 Vgt GND sky130_fd_pr__nfet_01v8 L=4 W=16 nf=1 ad='int((nf+1)/2) * W/nf * 0.29' as='int((nf+2)/2) * W/nf * 0.29'
+ pd='2*int((nf+1)/2) * (W/nf + 0.29)' ps='2*int((nf+2)/2) * (W/nf + 0.29)' nrd='0.29 / W' nrs='0.29 / W'
+ sa=0 sb=0 sd=0 mult=1 m=1
XM58 Vgt net10 net19 GND sky130_fd_pr__nfet_01v8 L=4 W=16 nf=1 ad='int((nf+1)/2) * W/nf * 0.29' as='int((nf+2)/2) * W/nf * 0.29'
+ pd='2*int((nf+1)/2) * (W/nf + 0.29)' ps='2*int((nf+2)/2) * (W/nf + 0.29)' nrd='0.29 / W' nrs='0.29 / W'
+ sa=0 sb=0 sd=0 mult=1 m=1
XMdumb59 Vgt GND GND GND sky130_fd_pr__nfet_01v8 L=4 W=16 nf=1 ad='int((nf+1)/2) * W/nf * 0.29' as='int((nf+2)/2) * W/nf * 0.29'
+ pd='2*int((nf+1)/2) * (W/nf + 0.29)' ps='2*int((nf+2)/2) * (W/nf + 0.29)' nrd='0.29 / W' nrs='0.29 / W'
+ sa=0 sb=0 sd=0 mult=1 m=1
XMdumb60 Vgt GND GND GND sky130_fd_pr__nfet_01v8 L=4 W=16 nf=1 ad='int((nf+1)/2) * W/nf * 0.29' as='int((nf+2)/2) * W/nf * 0.29'
+ pd='2*int((nf+1)/2) * (W/nf + 0.29)' ps='2*int((nf+2)/2) * (W/nf + 0.29)' nrd='0.29 / W' nrs='0.29 / W'
+ sa=0 sb=0 sd=0 mult=1 m=1
**** begin user architecture code

.option wnflag=1
.param MC_SWITCH=0.0
.lib ~/skywater/skywater-pdk/libraries/sky130_fd_pr_ngspice/latest/models/sky130.lib.spice tt


.control
dc Vdd 0 1.8 0.01
*save Vibias
save all
plot i(Vibias)
.endc
.OPTIONS ITL1=1000  ITL2=500 ITL6=500 GMINSTepS=200

**** end user architecture code
**.ends
.GLOBAL GND
.GLOBAL VDD
.end
